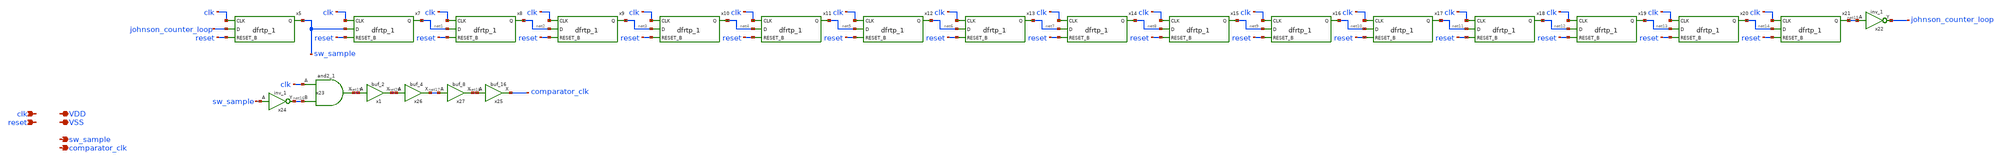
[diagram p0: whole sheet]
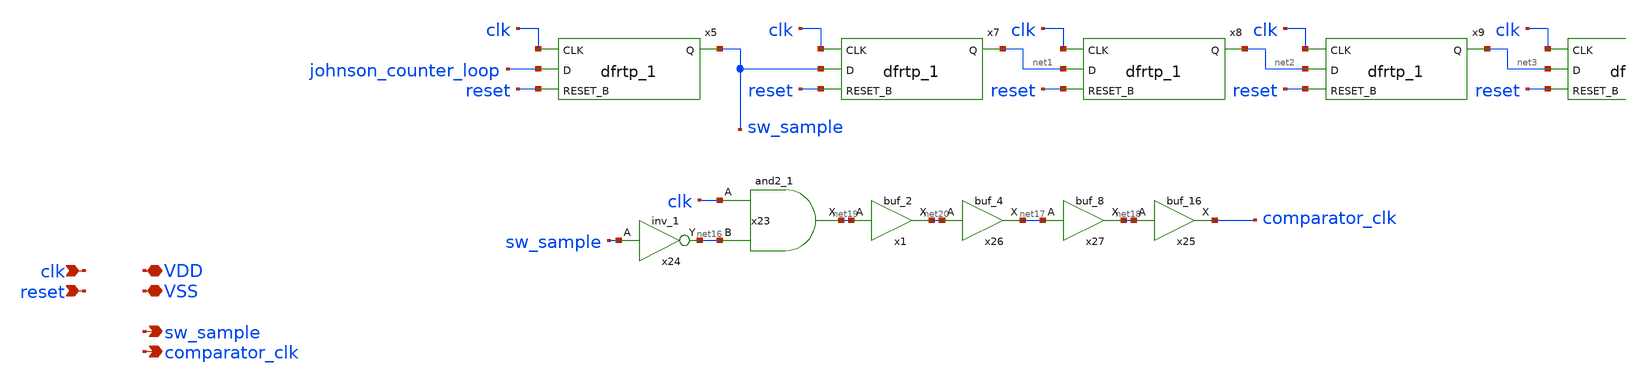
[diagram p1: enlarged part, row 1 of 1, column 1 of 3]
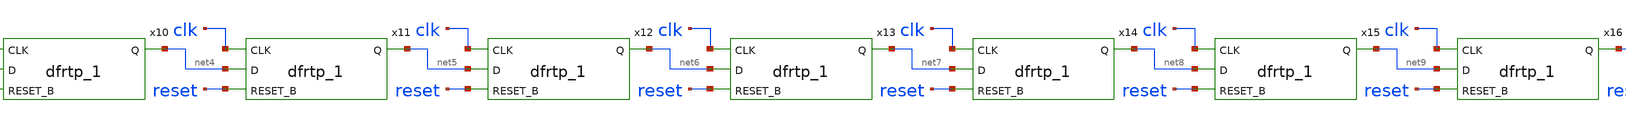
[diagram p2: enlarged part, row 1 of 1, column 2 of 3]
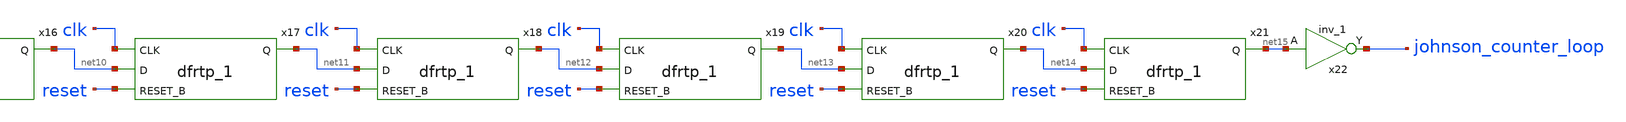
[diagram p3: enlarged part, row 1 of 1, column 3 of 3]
** sch_path: xschem/src/sample_clock/sample_clock.sch
**.subckt sample_clock VDD clk sw_sample VSS comparator_clk reset
*.iopin VDD
*.ipin clk
*.opin sw_sample
*.iopin VSS
*.opin comparator_clk
*.ipin reset
x5 clk johnson_counter_loop reset VSS VSS VDD VDD sw_sample sky130_fd_sc_hd__dfrtp_1
x7 clk sw_sample reset VSS VSS VDD VDD net1 sky130_fd_sc_hd__dfrtp_1
x8 clk net1 reset VSS VSS VDD VDD net2 sky130_fd_sc_hd__dfrtp_1
x9 clk net2 reset VSS VSS VDD VDD net3 sky130_fd_sc_hd__dfrtp_1
x10 clk net3 reset VSS VSS VDD VDD net4 sky130_fd_sc_hd__dfrtp_1
x11 clk net4 reset VSS VSS VDD VDD net5 sky130_fd_sc_hd__dfrtp_1
x12 clk net5 reset VSS VSS VDD VDD net6 sky130_fd_sc_hd__dfrtp_1
x13 clk net6 reset VSS VSS VDD VDD net7 sky130_fd_sc_hd__dfrtp_1
x14 clk net7 reset VSS VSS VDD VDD net8 sky130_fd_sc_hd__dfrtp_1
x15 clk net8 reset VSS VSS VDD VDD net9 sky130_fd_sc_hd__dfrtp_1
x16 clk net9 reset VSS VSS VDD VDD net10 sky130_fd_sc_hd__dfrtp_1
x17 clk net10 reset VSS VSS VDD VDD net11 sky130_fd_sc_hd__dfrtp_1
x18 clk net11 reset VSS VSS VDD VDD net12 sky130_fd_sc_hd__dfrtp_1
x19 clk net12 reset VSS VSS VDD VDD net13 sky130_fd_sc_hd__dfrtp_1
x20 clk net13 reset VSS VSS VDD VDD net14 sky130_fd_sc_hd__dfrtp_1
x21 clk net14 reset VSS VSS VDD VDD net15 sky130_fd_sc_hd__dfrtp_1
x22 net15 VSS VSS VDD VDD johnson_counter_loop sky130_fd_sc_hd__inv_1
x23 clk net16 VSS VSS VDD VDD net19 sky130_fd_sc_hd__and2_1
x24 sw_sample VSS VSS VDD VDD net16 sky130_fd_sc_hd__inv_1
x25 net18 VSS VSS VDD VDD comparator_clk sky130_fd_sc_hd__buf_16
x26 net20 VSS VSS VDD VDD net17 sky130_fd_sc_hd__buf_4
x27 net17 VSS VSS VDD VDD net18 sky130_fd_sc_hd__buf_8
x1 net19 VSS VSS VDD VDD net20 sky130_fd_sc_hd__buf_2
**.ends
.end
